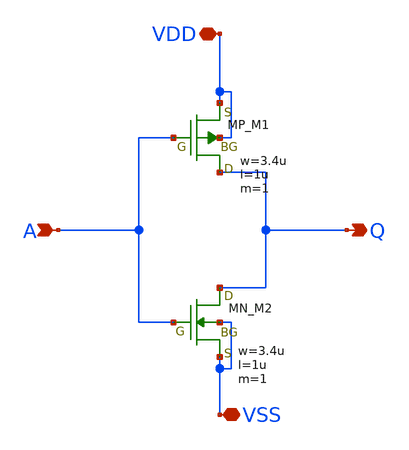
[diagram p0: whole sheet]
** sch_path: member_project/ringOSC/noritsuna/inverter_kudo.sch
**.subckt inverter_kudo A Q VDD VSS
*.ipin A
*.opin Q
*.iopin VDD
*.iopin VSS
XM1 Q A VDD VDD PMOS w=3.4u l=1u as=0 ad=0 ps=0 pd=0 nrd=0 nrs=0 m=1
XM2 Q A VSS VSS NMOS w=3.4u l=1u as=0 ad=0 ps=0 pd=0 nrd=0 nrs=0 m=1
**.ends
.end
